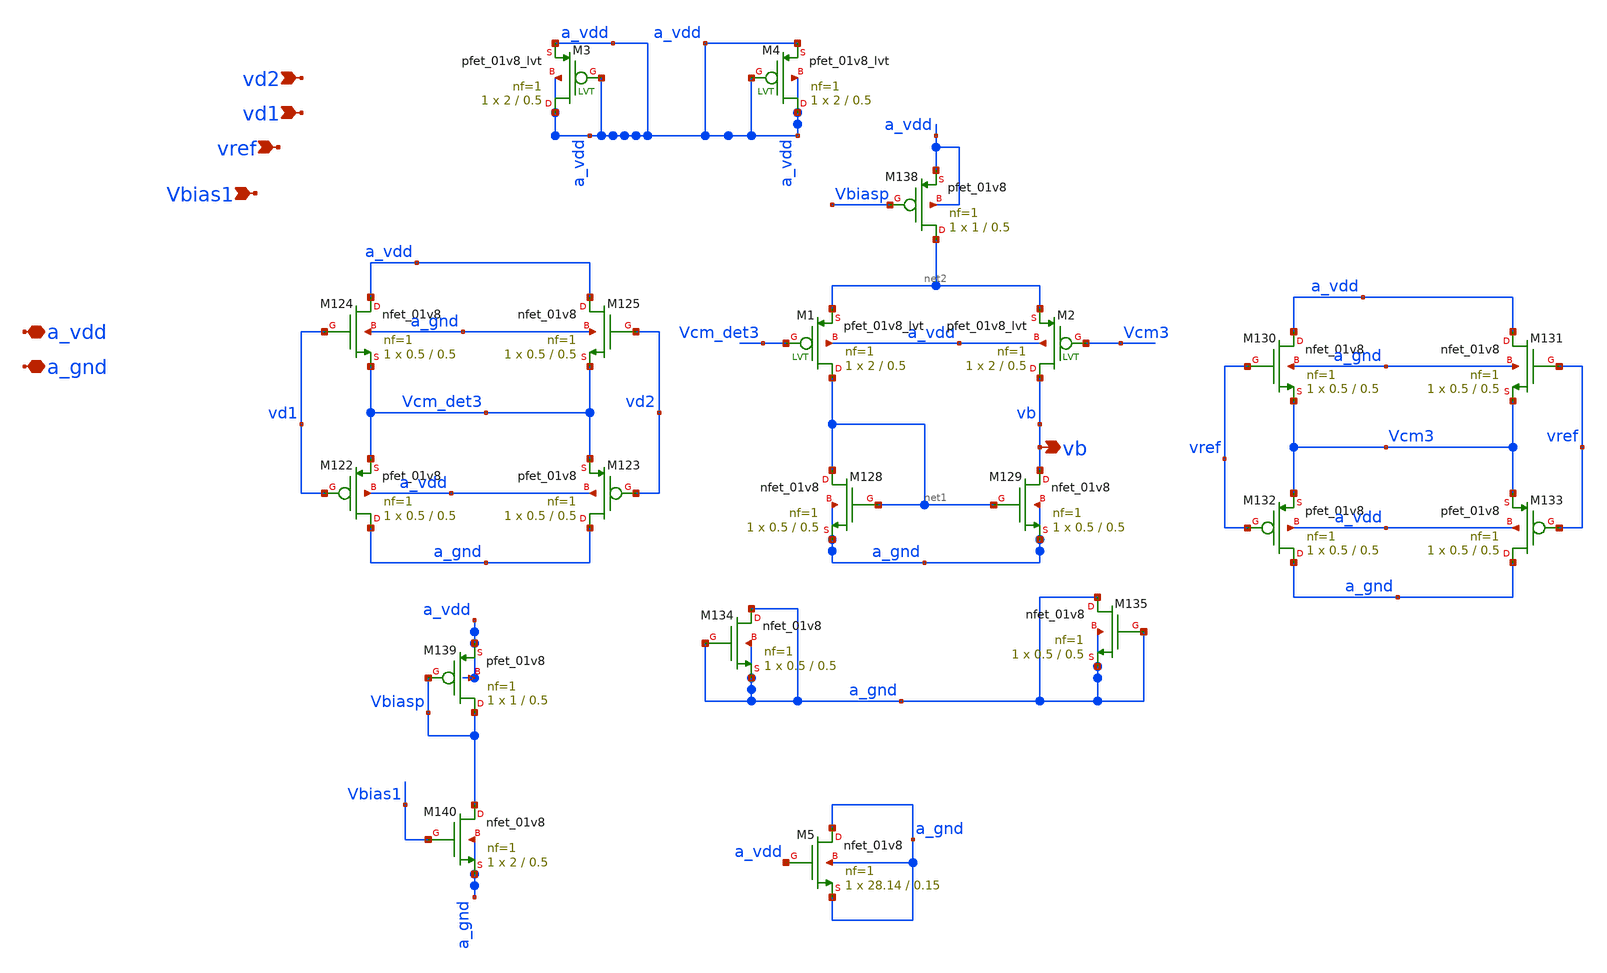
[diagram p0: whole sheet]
** sch_path: xschem/charge_pumps2/charge_pump_cmfb.sch
**.subckt charge_pump_cmfb a_gnd a_vdd vd1 vref vd2 vb Vbias1
*.iopin a_gnd
*.iopin a_vdd
*.ipin vd1
*.ipin vref
*.ipin vd2
*.opin vb
*.ipin Vbias1
XM122 a_gnd vd1 Vcm_det3 a_vdd sky130_fd_pr__pfet_01v8 L=0.5 W=0.5 nf=1 ad='int((nf+1)/2) * W/nf * 0.29'
+ as='int((nf+2)/2) * W/nf * 0.29' pd='2*int((nf+1)/2) * (W/nf + 0.29)' ps='2*int((nf+2)/2) * (W/nf + 0.29)'
+ nrd='0.29 / W' nrs='0.29 / W' sa=0 sb=0 sd=0 mult=1 m=1
XM123 a_gnd vd2 Vcm_det3 a_vdd sky130_fd_pr__pfet_01v8 L=0.5 W=0.5 nf=1 ad='int((nf+1)/2) * W/nf * 0.29'
+ as='int((nf+2)/2) * W/nf * 0.29' pd='2*int((nf+1)/2) * (W/nf + 0.29)' ps='2*int((nf+2)/2) * (W/nf + 0.29)'
+ nrd='0.29 / W' nrs='0.29 / W' sa=0 sb=0 sd=0 mult=1 m=1
XM124 a_vdd vd1 Vcm_det3 a_gnd sky130_fd_pr__nfet_01v8 L=0.5 W=0.5 nf=1 ad='int((nf+1)/2) * W/nf * 0.29'
+ as='int((nf+2)/2) * W/nf * 0.29' pd='2*int((nf+1)/2) * (W/nf + 0.29)' ps='2*int((nf+2)/2) * (W/nf + 0.29)'
+ nrd='0.29 / W' nrs='0.29 / W' sa=0 sb=0 sd=0 mult=1 m=1
XM125 a_vdd vd2 Vcm_det3 a_gnd sky130_fd_pr__nfet_01v8 L=0.5 W=0.5 nf=1 ad='int((nf+1)/2) * W/nf * 0.29'
+ as='int((nf+2)/2) * W/nf * 0.29' pd='2*int((nf+1)/2) * (W/nf + 0.29)' ps='2*int((nf+2)/2) * (W/nf + 0.29)'
+ nrd='0.29 / W' nrs='0.29 / W' sa=0 sb=0 sd=0 mult=1 m=1
XM128 net1 net1 a_gnd a_gnd sky130_fd_pr__nfet_01v8 L=0.5 W=0.5 nf=1 ad='int((nf+1)/2) * W/nf * 0.29'
+ as='int((nf+2)/2) * W/nf * 0.29' pd='2*int((nf+1)/2) * (W/nf + 0.29)' ps='2*int((nf+2)/2) * (W/nf + 0.29)'
+ nrd='0.29 / W' nrs='0.29 / W' sa=0 sb=0 sd=0 mult=1 m=1
XM129 vb net1 a_gnd a_gnd sky130_fd_pr__nfet_01v8 L=0.5 W=0.5 nf=1 ad='int((nf+1)/2) * W/nf * 0.29' as='int((nf+2)/2) * W/nf * 0.29'
+ pd='2*int((nf+1)/2) * (W/nf + 0.29)' ps='2*int((nf+2)/2) * (W/nf + 0.29)' nrd='0.29 / W' nrs='0.29 / W'
+ sa=0 sb=0 sd=0 mult=1 m=1
XM130 a_vdd vref Vcm3 a_gnd sky130_fd_pr__nfet_01v8 L=0.5 W=0.5 nf=1 ad='int((nf+1)/2) * W/nf * 0.29'
+ as='int((nf+2)/2) * W/nf * 0.29' pd='2*int((nf+1)/2) * (W/nf + 0.29)' ps='2*int((nf+2)/2) * (W/nf + 0.29)'
+ nrd='0.29 / W' nrs='0.29 / W' sa=0 sb=0 sd=0 mult=1 m=1
XM131 a_vdd vref Vcm3 a_gnd sky130_fd_pr__nfet_01v8 L=0.5 W=0.5 nf=1 ad='int((nf+1)/2) * W/nf * 0.29'
+ as='int((nf+2)/2) * W/nf * 0.29' pd='2*int((nf+1)/2) * (W/nf + 0.29)' ps='2*int((nf+2)/2) * (W/nf + 0.29)'
+ nrd='0.29 / W' nrs='0.29 / W' sa=0 sb=0 sd=0 mult=1 m=1
XM132 a_gnd vref Vcm3 a_vdd sky130_fd_pr__pfet_01v8 L=0.5 W=0.5 nf=1 ad='int((nf+1)/2) * W/nf * 0.29'
+ as='int((nf+2)/2) * W/nf * 0.29' pd='2*int((nf+1)/2) * (W/nf + 0.29)' ps='2*int((nf+2)/2) * (W/nf + 0.29)'
+ nrd='0.29 / W' nrs='0.29 / W' sa=0 sb=0 sd=0 mult=1 m=1
XM133 a_gnd vref Vcm3 a_vdd sky130_fd_pr__pfet_01v8 L=0.5 W=0.5 nf=1 ad='int((nf+1)/2) * W/nf * 0.29'
+ as='int((nf+2)/2) * W/nf * 0.29' pd='2*int((nf+1)/2) * (W/nf + 0.29)' ps='2*int((nf+2)/2) * (W/nf + 0.29)'
+ nrd='0.29 / W' nrs='0.29 / W' sa=0 sb=0 sd=0 mult=1 m=1
XM134 a_gnd a_gnd a_gnd a_gnd sky130_fd_pr__nfet_01v8 L=0.5 W=0.5 nf=1 ad='int((nf+1)/2) * W/nf * 0.29'
+ as='int((nf+2)/2) * W/nf * 0.29' pd='2*int((nf+1)/2) * (W/nf + 0.29)' ps='2*int((nf+2)/2) * (W/nf + 0.29)'
+ nrd='0.29 / W' nrs='0.29 / W' sa=0 sb=0 sd=0 mult=1 m=1
XM135 a_gnd a_gnd a_gnd a_gnd sky130_fd_pr__nfet_01v8 L=0.5 W=0.5 nf=1 ad='int((nf+1)/2) * W/nf * 0.29'
+ as='int((nf+2)/2) * W/nf * 0.29' pd='2*int((nf+1)/2) * (W/nf + 0.29)' ps='2*int((nf+2)/2) * (W/nf + 0.29)'
+ nrd='0.29 / W' nrs='0.29 / W' sa=0 sb=0 sd=0 mult=1 m=1
XM138 net2 Vbiasp a_vdd a_vdd sky130_fd_pr__pfet_01v8 L=0.5 W=1 nf=1 ad='int((nf+1)/2) * W/nf * 0.29'
+ as='int((nf+2)/2) * W/nf * 0.29' pd='2*int((nf+1)/2) * (W/nf + 0.29)' ps='2*int((nf+2)/2) * (W/nf + 0.29)'
+ nrd='0.29 / W' nrs='0.29 / W' sa=0 sb=0 sd=0 mult=1 m=1
XM139 Vbiasp Vbiasp a_vdd a_vdd sky130_fd_pr__pfet_01v8 L=0.5 W=1 nf=1 ad='int((nf+1)/2) * W/nf * 0.29'
+ as='int((nf+2)/2) * W/nf * 0.29' pd='2*int((nf+1)/2) * (W/nf + 0.29)' ps='2*int((nf+2)/2) * (W/nf + 0.29)'
+ nrd='0.29 / W' nrs='0.29 / W' sa=0 sb=0 sd=0 mult=1 m=1
XM140 Vbiasp Vbias1 a_gnd a_gnd sky130_fd_pr__nfet_01v8 L=0.5 W=2 nf=1 ad='int((nf+1)/2) * W/nf * 0.29'
+ as='int((nf+2)/2) * W/nf * 0.29' pd='2*int((nf+1)/2) * (W/nf + 0.29)' ps='2*int((nf+2)/2) * (W/nf + 0.29)'
+ nrd='0.29 / W' nrs='0.29 / W' sa=0 sb=0 sd=0 mult=1 m=1
XM1 net1 Vcm_det3 net2 a_vdd sky130_fd_pr__pfet_01v8_lvt L=0.5 W=2 nf=1 ad='int((nf+1)/2) * W/nf * 0.29'
+ as='int((nf+2)/2) * W/nf * 0.29' pd='2*int((nf+1)/2) * (W/nf + 0.29)' ps='2*int((nf+2)/2) * (W/nf + 0.29)'
+ nrd='0.29 / W' nrs='0.29 / W' sa=0 sb=0 sd=0 mult=1 m=1
XM2 vb Vcm3 net2 a_vdd sky130_fd_pr__pfet_01v8_lvt L=0.5 W=2 nf=1 ad='int((nf+1)/2) * W/nf * 0.29' as='int((nf+2)/2) * W/nf * 0.29'
+ pd='2*int((nf+1)/2) * (W/nf + 0.29)' ps='2*int((nf+2)/2) * (W/nf + 0.29)' nrd='0.29 / W' nrs='0.29 / W'
+ sa=0 sb=0 sd=0 mult=1 m=1
XM3 a_vdd a_vdd a_vdd a_vdd sky130_fd_pr__pfet_01v8_lvt L=0.5 W=2 nf=1 ad='int((nf+1)/2) * W/nf * 0.29'
+ as='int((nf+2)/2) * W/nf * 0.29' pd='2*int((nf+1)/2) * (W/nf + 0.29)' ps='2*int((nf+2)/2) * (W/nf + 0.29)'
+ nrd='0.29 / W' nrs='0.29 / W' sa=0 sb=0 sd=0 mult=1 m=1
XM4 a_vdd a_vdd a_vdd a_vdd sky130_fd_pr__pfet_01v8_lvt L=0.5 W=2 nf=1 ad='int((nf+1)/2) * W/nf * 0.29'
+ as='int((nf+2)/2) * W/nf * 0.29' pd='2*int((nf+1)/2) * (W/nf + 0.29)' ps='2*int((nf+2)/2) * (W/nf + 0.29)'
+ nrd='0.29 / W' nrs='0.29 / W' sa=0 sb=0 sd=0 mult=1 m=1
XM5 a_gnd a_vdd a_gnd a_gnd sky130_fd_pr__nfet_01v8 L=0.15 W=28.14 nf=1 ad='int((nf+1)/2) * W/nf * 0.29'
+ as='int((nf+2)/2) * W/nf * 0.29' pd='2*int((nf+1)/2) * (W/nf + 0.29)' ps='2*int((nf+2)/2) * (W/nf + 0.29)'
+ nrd='0.29 / W' nrs='0.29 / W' sa=0 sb=0 sd=0 mult=1 m=1
**.ends
.end
